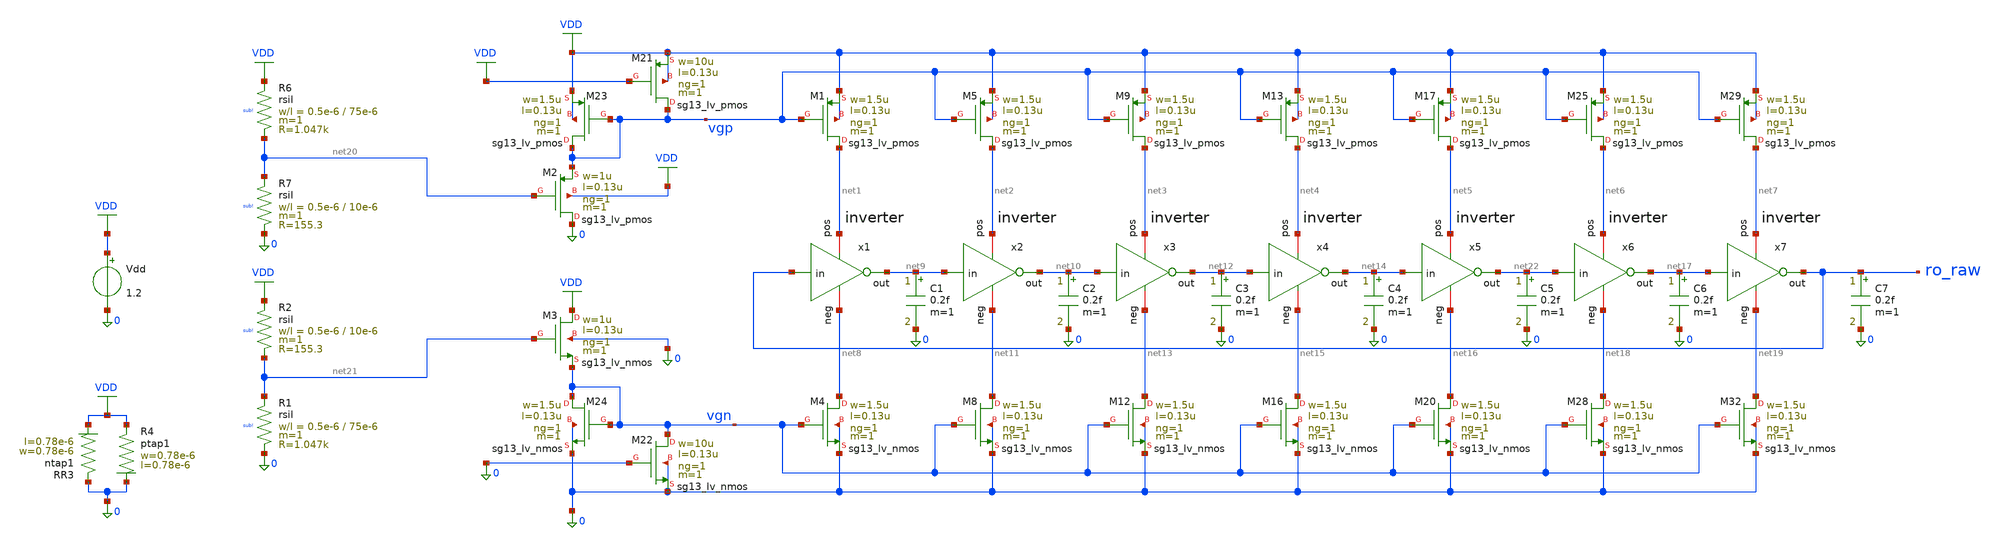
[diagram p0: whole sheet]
** sch_path: analog/temp-sens-core/temp-sens-core.sch
**.subckt temp-sens-core
XM1 net1 vgp VDD VDD sg13_lv_pmos w=1.5u l=0.13u ng=1 m=1 mm_ok=1
XM21 vgp VDD VDD VDD sg13_lv_pmos w=10u l=0.13u ng=1 m=1 mm_ok=1
XM22 vgn 0 0 0 sg13_lv_nmos w=10u l=0.13u ng=1 m=1 mm_ok=1
XM23 vgp vgp VDD VDD sg13_lv_pmos w=1.5u l=0.13u ng=1 m=1 mm_ok=1
XM24 vgn vgn 0 0 sg13_lv_nmos w=1.5u l=0.13u ng=1 m=1 mm_ok=1
Vdd VDD 0 1.2
XR3 0 VDD ntap1 R=262.8 w=0.78e-6 l=0.78e-6
XR4 VDD 0 ptap1 R=262.8 w=0.78e-6 l=0.78e-6
XM4 net8 vgn 0 0 sg13_lv_nmos w=1.5u l=0.13u ng=1 m=1 mm_ok=1
XM5 net2 vgp VDD VDD sg13_lv_pmos w=1.5u l=0.13u ng=1 m=1 mm_ok=1
XM8 net11 vgn 0 0 sg13_lv_nmos w=1.5u l=0.13u ng=1 m=1 mm_ok=1
XM9 net3 vgp VDD VDD sg13_lv_pmos w=1.5u l=0.13u ng=1 m=1 mm_ok=1
XM12 net13 vgn 0 0 sg13_lv_nmos w=1.5u l=0.13u ng=1 m=1 mm_ok=1
XM13 net4 vgp VDD VDD sg13_lv_pmos w=1.5u l=0.13u ng=1 m=1 mm_ok=1
XM16 net15 vgn 0 0 sg13_lv_nmos w=1.5u l=0.13u ng=1 m=1 mm_ok=1
XM17 net5 vgp VDD VDD sg13_lv_pmos w=1.5u l=0.13u ng=1 m=1 mm_ok=1
XM20 net16 vgn 0 0 sg13_lv_nmos w=1.5u l=0.13u ng=1 m=1 mm_ok=1
XM25 net6 vgp VDD VDD sg13_lv_pmos w=1.5u l=0.13u ng=1 m=1 mm_ok=1
XM28 net18 vgn 0 0 sg13_lv_nmos w=1.5u l=0.13u ng=1 m=1 mm_ok=1
XM29 net7 vgp VDD VDD sg13_lv_pmos w=1.5u l=0.13u ng=1 m=1 mm_ok=1
XM32 net19 vgn 0 0 sg13_lv_nmos w=1.5u l=0.13u ng=1 m=1 mm_ok=1
x1 net1 ro_raw net9 net8 inverter
x2 net2 net9 net10 net11 inverter
x3 net3 net10 net12 net13 inverter
x4 net4 net12 net14 net15 inverter
x5 net5 net14 net22 net16 inverter
x6 net6 net22 net17 net18 inverter
x7 net7 net17 ro_raw net19 inverter
XM2 0 net20 vgp VDD sg13_lv_pmos w=1u l=0.13u ng=1 m=1 mm_ok=1
XM3 VDD net21 vgn 0 sg13_lv_nmos w=1u l=0.13u ng=1 m=1 mm_ok=1
XR6 VDD net20 sub! rsil w=0.5e-6 l=75e-6 m=1 mm_ok=1
XR7 net20 0 sub! rsil w=0.5e-6 l=10e-6 m=1 mm_ok=1
XR1 net21 0 sub! rsil w=0.5e-6 l=75e-6 m=1 mm_ok=1
XR2 VDD net21 sub! rsil w=0.5e-6 l=10e-6 m=1 mm_ok=1
C1 net9 0 0.2f m=1
C2 net10 0 0.2f m=1
C3 net12 0 0.2f m=1
C4 net14 0 0.2f m=1
C5 net22 0 0.2f m=1
C6 net17 0 0.2f m=1
C7 ro_raw 0 0.2f m=1
**** begin user architecture code



* ngspice commands
.option rshunt=1e12
.option klu
.control

let temp_start = 15
let temp_stop = 35
let temp_delta = 5

* Create one plot that will hold the sweep results
setplot new
set scratch = $curplot

compose temperature start=$&temp_start stop=$&temp_stop step=$&temp_delta
let frequency = vector(length(temperature))

let i = 0
let tcur = temp_start
while $&tcur le $&temp_stop
  option temp = $&tcur

  tran 0.05n 300n

  meas tran tperiod
  + TRIG v(ro_raw) VAL=0.6 RISE=2 TD=50n
  + TARG v(ro_raw) VAL=0.6 RISE=3 TD=50n

  * Remember the just-created tran plot
  set dt = $curplot

  * Go back to the scratch plot before touching loop variables
  setplot $scratch

  let frequency[i] = 1/{$dt}.tperiod

  if $&tcur eq 25
    let time25 = {$dt}.time
    let ro_raw25 = {$dt}.v(ro_raw)
  end

  let tcur = tcur + temp_delta
  let i = i+1
end

setplot $scratch

settype temp-sweep temperature
settype frequency frequency
setscale frequency temperature
write temp-sweep_sens-core.raw temperature frequency

settype time time25
settype voltage ro_raw25
setscale ro_raw25 time25
write temp25_wave.raw time25 ro_raw25
.endc






.lib cornerMOSlv.lib mos_tt
.lib cornerMOShv.lib mos_tt
.lib cornerRES.lib res_typ
.lib cornerDIO.lib dio_tt






.include /foss/pdks/ihp-sg13cmos5l/libs.ref/sg13cmos5l_stdcell/spice/sg13cmos5l_stdcell.spice



**** end user architecture code
**.ends

* expanding   symbol:  analog/inverter/inverter.sym # of pins=4
** sym_path: analog/inverter/inverter.sym
** sch_path: analog/inverter/inverter.sch
.subckt inverter pos in out neg
*.ipin in
*.iopin pos
*.iopin neg
*.opin out
XM1 out in neg neg sg13_lv_nmos w=2.0u l=0.45u ng=1 m=1 mm_ok=1
XM2 pos in out pos sg13_lv_pmos w=1.0u l=0.45u ng=1 m=1 mm_ok=1
.ends

.GLOBAL VDD
.end
